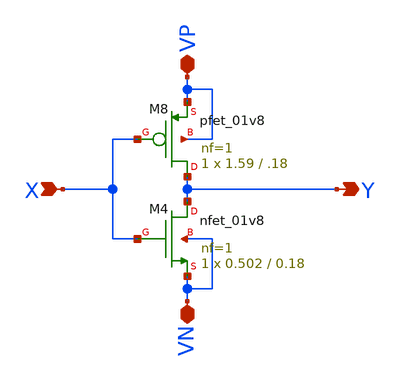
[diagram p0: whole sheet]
** sch_path: component/black_inv_1/black_inv.sch
**.subckt black_inv X Y VN VP
*.ipin X
*.opin Y
*.iopin VN
*.iopin VP
XM8 Y X VP VP sky130_fd_pr__pfet_01v8 L=.18 W=1.59 nf=1 ad='int((nf+1)/2) * W/nf * 0.29' as='int((nf+2)/2) * W/nf * 0.29'
+ pd='2*int((nf+1)/2) * (W/nf + 0.29)' ps='2*int((nf+2)/2) * (W/nf + 0.29)' nrd='0.29 / W' nrs='0.29 / W'
+ sa=0 sb=0 sd=0 mult=1 m=1
XM4 Y X VN VN sky130_fd_pr__nfet_01v8 L=0.18 W=0.502 nf=1 ad='int((nf+1)/2) * W/nf * 0.29' as='int((nf+2)/2) * W/nf * 0.29'
+ pd='2*int((nf+1)/2) * (W/nf + 0.29)' ps='2*int((nf+2)/2) * (W/nf + 0.29)' nrd='0.29 / W' nrs='0.29 / W'
+ sa=0 sb=0 sd=0 mult=1 m=1
**.ends
.end
